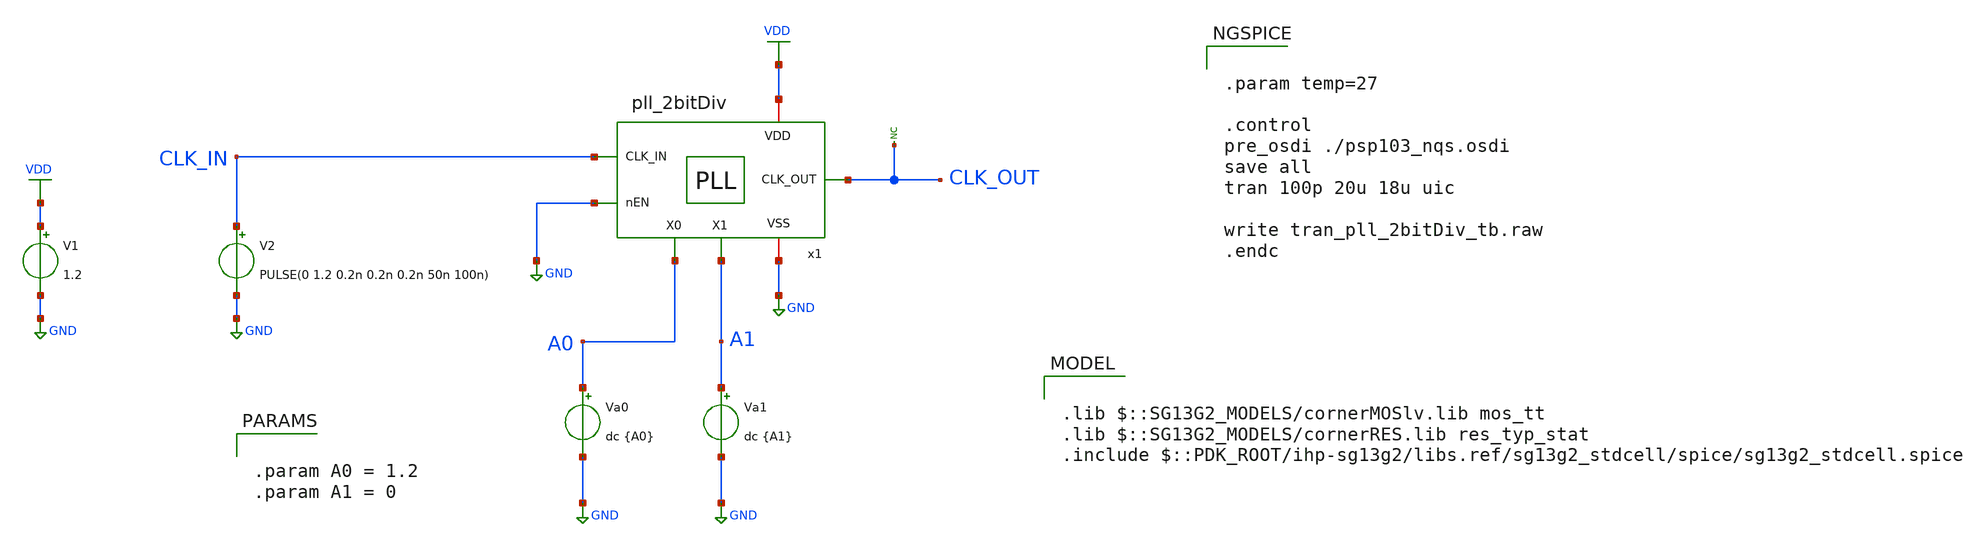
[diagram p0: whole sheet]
** sch_path: Combined Design/design_data/xschem/pll_2bitDiv_tb.sch

.lib $::SG13G2_MODELS/cornerMOSlv.lib mos_tt
.lib $::SG13G2_MODELS/cornerRES.lib res_typ_stat
.include $::PDK_ROOT/ihp-sg13g2/libs.ref/sg13g2_stdcell/spice/sg13g2_stdcell.spice

**.subckt pll_2bitDiv_tb
V1 VDD GND 1.2
V2 CLK_IN GND PULSE(0 1.2 0.2n 0.2n 0.2n 50n 100n)
x1 CLK_IN CLK_OUT VDD GND GND A1 A0 pll_2bitDiv
Va0 A0 GND dc {A0}
Va1 A1 GND dc {A1}
* noconn CLK_OUT
**** begin user architecture code


.param temp=27

.control
pre_osdi ./psp103_nqs.osdi
save all
tran 100p 20u 18u uic

write tran_pll_2bitDiv_tb.raw
.endc





.meas tran tperiod_in TRIG v(clk_in) VAL=0.6 FALL=1 TARG v(clk_in) VAL=0.6 FALL=2
.meas tran ref_freq PARAM = '1e-6/tperiod_in'

.meas tran tperiod_out TRIG v(clk_out) VAL=0.6 FALL=1 TARG v(clk_out) VAL=0.6 FALL=2
.meas tran pll_freq PARAM = '1e-6/tperiod_out'




.param A0 = 1.2
.param A1 = 0


**** end user architecture code
**.ends
.GLOBAL GND
.GLOBAL VDD
.end
